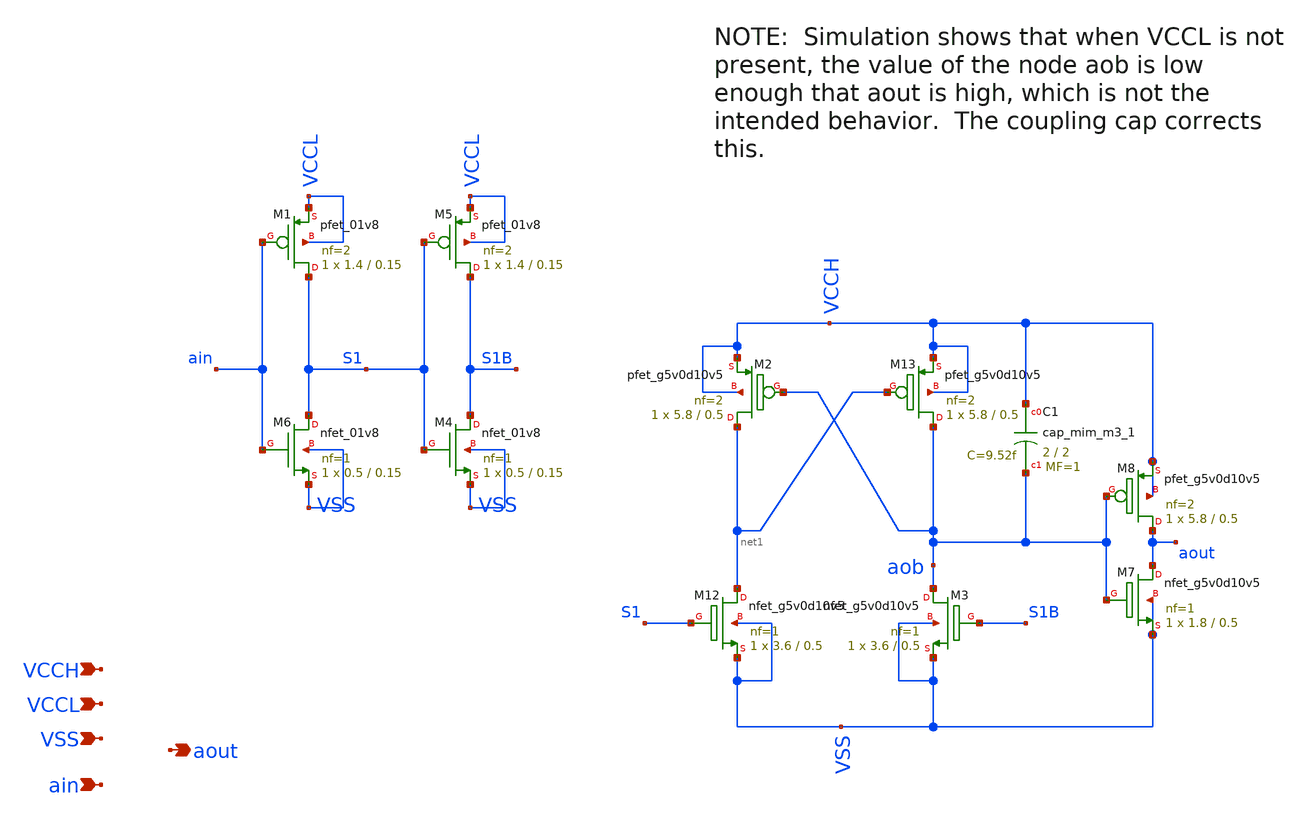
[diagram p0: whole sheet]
** sch_path: xschem/levelShifter.sch
**.subckt levelShifter VCCL VSS ain aout VCCH
*.ipin VCCL
*.ipin VSS
*.ipin ain
*.opin aout
*.ipin VCCH
XM12 net1 S1 VSS VSS sky130_fd_pr__nfet_g5v0d10v5 L=0.5 W=3.6 nf=1 ad='int((nf+1)/2) * W/nf * 0.29' as='int((nf+2)/2) * W/nf * 0.29'
+ pd='2*int((nf+1)/2) * (W/nf + 0.29)' ps='2*int((nf+2)/2) * (W/nf + 0.29)' nrd='0.29 / W' nrs='0.29 / W'
+ sa=0 sb=0 sd=0 mult=1 m=1
XM13 aob net1 VCCH VCCH sky130_fd_pr__pfet_g5v0d10v5 L=0.5 W=5.8 nf=2 ad='int((nf+1)/2) * W/nf * 0.29'
+ as='int((nf+2)/2) * W/nf * 0.29' pd='2*int((nf+1)/2) * (W/nf + 0.29)' ps='2*int((nf+2)/2) * (W/nf + 0.29)'
+ nrd='0.29 / W' nrs='0.29 / W' sa=0 sb=0 sd=0 mult=1 m=1
XM6 S1 ain VSS VSS sky130_fd_pr__nfet_01v8 L=0.15 W=0.5 nf=1 ad='int((nf+1)/2) * W/nf * 0.29' as='int((nf+2)/2) * W/nf * 0.29'
+ pd='2*int((nf+1)/2) * (W/nf + 0.29)' ps='2*int((nf+2)/2) * (W/nf + 0.29)' nrd='0.29 / W' nrs='0.29 / W'
+ sa=0 sb=0 sd=0 mult=1 m=1
XM1 S1 ain VCCL VCCL sky130_fd_pr__pfet_01v8 L=0.15 W=1.4 nf=2 ad='int((nf+1)/2) * W/nf * 0.29' as='int((nf+2)/2) * W/nf * 0.29'
+ pd='2*int((nf+1)/2) * (W/nf + 0.29)' ps='2*int((nf+2)/2) * (W/nf + 0.29)' nrd='0.29 / W' nrs='0.29 / W'
+ sa=0 sb=0 sd=0 mult=1 m=1
XM2 net1 aob VCCH VCCH sky130_fd_pr__pfet_g5v0d10v5 L=0.5 W=5.8 nf=2 ad='int((nf+1)/2) * W/nf * 0.29'
+ as='int((nf+2)/2) * W/nf * 0.29' pd='2*int((nf+1)/2) * (W/nf + 0.29)' ps='2*int((nf+2)/2) * (W/nf + 0.29)'
+ nrd='0.29 / W' nrs='0.29 / W' sa=0 sb=0 sd=0 mult=1 m=1
XM3 aob S1B VSS VSS sky130_fd_pr__nfet_g5v0d10v5 L=0.5 W=3.6 nf=1 ad='int((nf+1)/2) * W/nf * 0.29' as='int((nf+2)/2) * W/nf * 0.29'
+ pd='2*int((nf+1)/2) * (W/nf + 0.29)' ps='2*int((nf+2)/2) * (W/nf + 0.29)' nrd='0.29 / W' nrs='0.29 / W'
+ sa=0 sb=0 sd=0 mult=1 m=1
XM4 S1B S1 VSS VSS sky130_fd_pr__nfet_01v8 L=0.15 W=0.5 nf=1 ad='int((nf+1)/2) * W/nf * 0.29' as='int((nf+2)/2) * W/nf * 0.29'
+ pd='2*int((nf+1)/2) * (W/nf + 0.29)' ps='2*int((nf+2)/2) * (W/nf + 0.29)' nrd='0.29 / W' nrs='0.29 / W'
+ sa=0 sb=0 sd=0 mult=1 m=1
XM5 S1B S1 VCCL VCCL sky130_fd_pr__pfet_01v8 L=0.15 W=1.4 nf=2 ad='int((nf+1)/2) * W/nf * 0.29' as='int((nf+2)/2) * W/nf * 0.29'
+ pd='2*int((nf+1)/2) * (W/nf + 0.29)' ps='2*int((nf+2)/2) * (W/nf + 0.29)' nrd='0.29 / W' nrs='0.29 / W'
+ sa=0 sb=0 sd=0 mult=1 m=1
XM7 aout aob VSS VSS sky130_fd_pr__nfet_g5v0d10v5 L=0.5 W=1.8 nf=1 ad='int((nf+1)/2) * W/nf * 0.29' as='int((nf+2)/2) * W/nf * 0.29'
+ pd='2*int((nf+1)/2) * (W/nf + 0.29)' ps='2*int((nf+2)/2) * (W/nf + 0.29)' nrd='0.29 / W' nrs='0.29 / W'
+ sa=0 sb=0 sd=0 mult=1 m=1
XM8 aout aob VCCH VCCH sky130_fd_pr__pfet_g5v0d10v5 L=0.5 W=5.8 nf=2 ad='int((nf+1)/2) * W/nf * 0.29'
+ as='int((nf+2)/2) * W/nf * 0.29' pd='2*int((nf+1)/2) * (W/nf + 0.29)' ps='2*int((nf+2)/2) * (W/nf + 0.29)'
+ nrd='0.29 / W' nrs='0.29 / W' sa=0 sb=0 sd=0 mult=1 m=1
XC1 VCCH aob sky130_fd_pr__cap_mim_m3_1 W=2 L=2 MF=1 m=1
**.ends
.end
